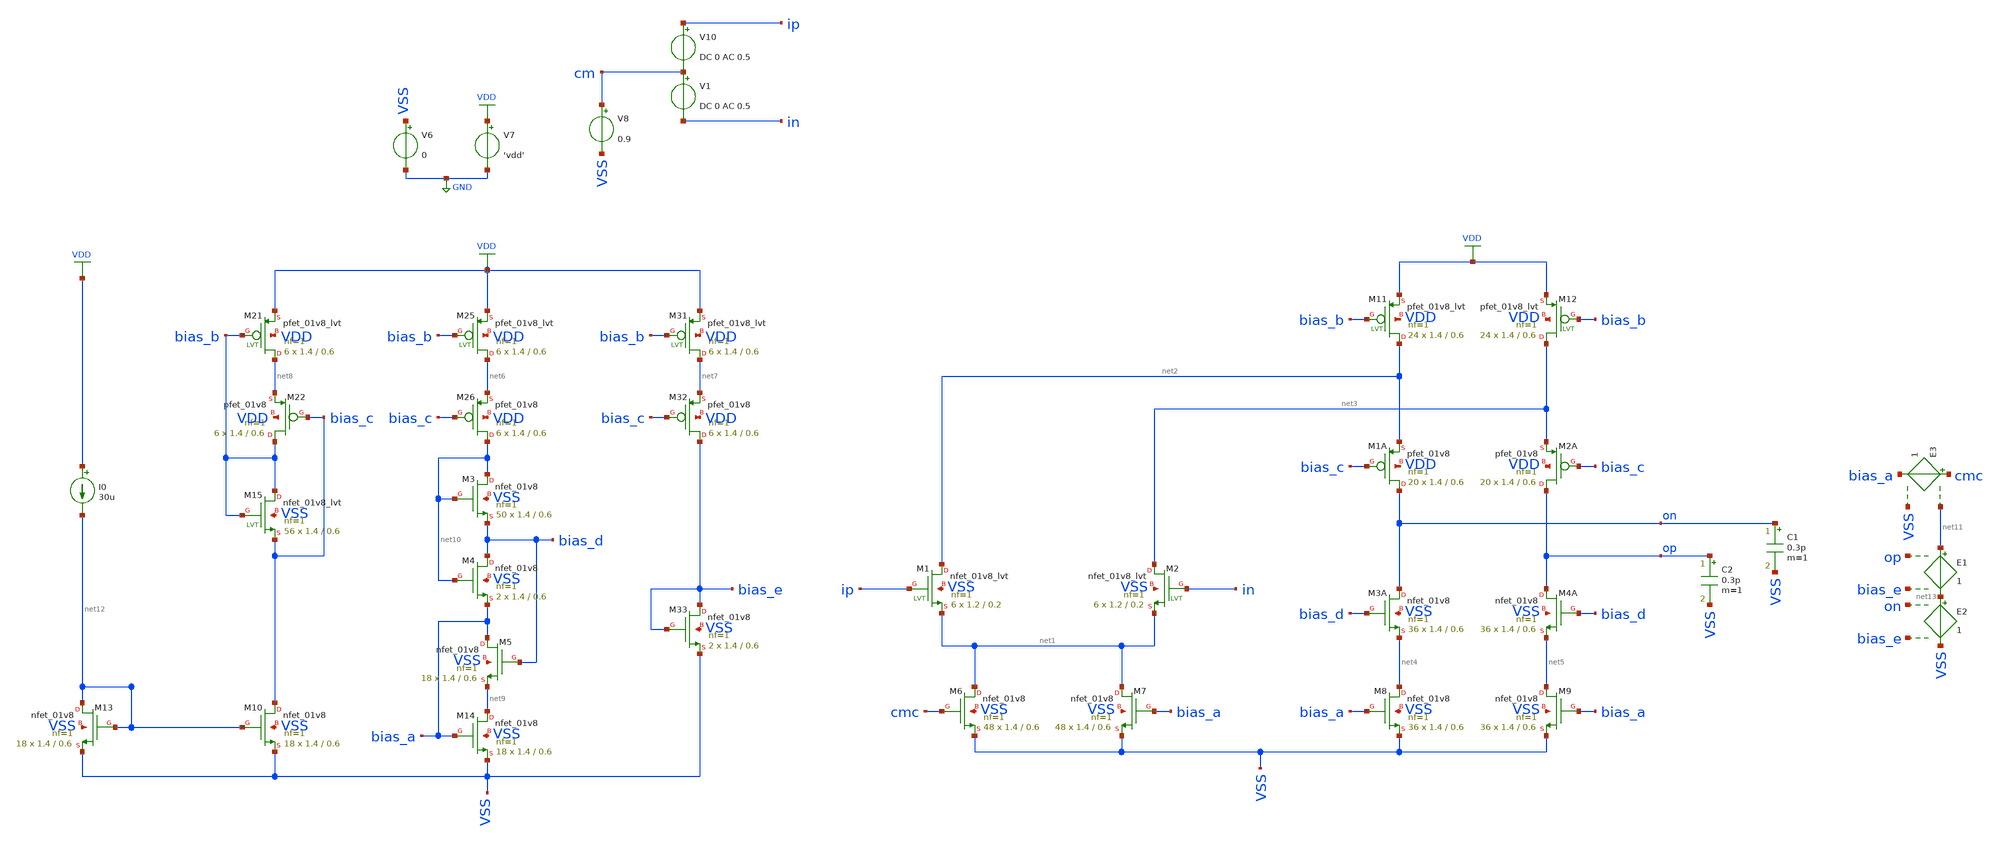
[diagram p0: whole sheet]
** sch_path: verification/schematic/folded_cascode_pvt_tb.sch
**.subckt folded_cascode_pvt_tb
XM1 net2 ip net1 VSS sky130_fd_pr__nfet_01v8_lvt L=0.2 W=1.2 nf=1 ad='int((nf+1)/2) * W/nf * 0.29' as='int((nf+2)/2) * W/nf * 0.29'
+ pd='2*int((nf+1)/2) * (W/nf + 0.29)' ps='2*int((nf+2)/2) * (W/nf + 0.29)' nrd='0.29 / W' nrs='0.29 / W'
+ sa=0 sb=0 sd=0 mult=6 m=6
XM2 net3 in net1 VSS sky130_fd_pr__nfet_01v8_lvt L=0.2 W=1.2 nf=1 ad='int((nf+1)/2) * W/nf * 0.29' as='int((nf+2)/2) * W/nf * 0.29'
+ pd='2*int((nf+1)/2) * (W/nf + 0.29)' ps='2*int((nf+2)/2) * (W/nf + 0.29)' nrd='0.29 / W' nrs='0.29 / W'
+ sa=0 sb=0 sd=0 mult=6 m=6
XM6 net1 cmc VSS VSS sky130_fd_pr__nfet_01v8 L=0.6 W=1.4 nf=1 ad='int((nf+1)/2) * W/nf * 0.29' as='int((nf+2)/2) * W/nf * 0.29'
+ pd='2*int((nf+1)/2) * (W/nf + 0.29)' ps='2*int((nf+2)/2) * (W/nf + 0.29)' nrd='0.29 / W' nrs='0.29 / W'
+ sa=0 sb=0 sd=0 mult=48 m=48
XM7 net1 bias_a VSS VSS sky130_fd_pr__nfet_01v8 L=0.6 W=1.4 nf=1 ad='int((nf+1)/2) * W/nf * 0.29' as='int((nf+2)/2) * W/nf * 0.29'
+ pd='2*int((nf+1)/2) * (W/nf + 0.29)' ps='2*int((nf+2)/2) * (W/nf + 0.29)' nrd='0.29 / W' nrs='0.29 / W'
+ sa=0 sb=0 sd=0 mult=48 m=48
XM11 net2 bias_b VDD VDD sky130_fd_pr__pfet_01v8_lvt L=0.6 W=1.4 nf=1 ad='int((nf+1)/2) * W/nf * 0.29'
+ as='int((nf+2)/2) * W/nf * 0.29' pd='2*int((nf+1)/2) * (W/nf + 0.29)' ps='2*int((nf+2)/2) * (W/nf + 0.29)'
+ nrd='0.29 / W' nrs='0.29 / W' sa=0 sb=0 sd=0 mult=24 m=24
XM12 net3 bias_b VDD VDD sky130_fd_pr__pfet_01v8_lvt L=0.6 W=1.4 nf=1 ad='int((nf+1)/2) * W/nf * 0.29'
+ as='int((nf+2)/2) * W/nf * 0.29' pd='2*int((nf+1)/2) * (W/nf + 0.29)' ps='2*int((nf+2)/2) * (W/nf + 0.29)'
+ nrd='0.29 / W' nrs='0.29 / W' sa=0 sb=0 sd=0 mult=24 m=24
XM1A on bias_c net2 VDD sky130_fd_pr__pfet_01v8 L=0.6 W=1.4 nf=1 ad='int((nf+1)/2) * W/nf * 0.29' as='int((nf+2)/2) * W/nf * 0.29'
+ pd='2*int((nf+1)/2) * (W/nf + 0.29)' ps='2*int((nf+2)/2) * (W/nf + 0.29)' nrd='0.29 / W' nrs='0.29 / W'
+ sa=0 sb=0 sd=0 mult=20 m=20
XM2A op bias_c net3 VDD sky130_fd_pr__pfet_01v8 L=0.6 W=1.4 nf=1 ad='int((nf+1)/2) * W/nf * 0.29' as='int((nf+2)/2) * W/nf * 0.29'
+ pd='2*int((nf+1)/2) * (W/nf + 0.29)' ps='2*int((nf+2)/2) * (W/nf + 0.29)' nrd='0.29 / W' nrs='0.29 / W'
+ sa=0 sb=0 sd=0 mult=20 m=20
XM3A on bias_d net4 VSS sky130_fd_pr__nfet_01v8 L=0.6 W=1.4 nf=1 ad='int((nf+1)/2) * W/nf * 0.29' as='int((nf+2)/2) * W/nf * 0.29'
+ pd='2*int((nf+1)/2) * (W/nf + 0.29)' ps='2*int((nf+2)/2) * (W/nf + 0.29)' nrd='0.29 / W' nrs='0.29 / W'
+ sa=0 sb=0 sd=0 mult=36 m=36
XM4A op bias_d net5 VSS sky130_fd_pr__nfet_01v8 L=0.6 W=1.4 nf=1 ad='int((nf+1)/2) * W/nf * 0.29' as='int((nf+2)/2) * W/nf * 0.29'
+ pd='2*int((nf+1)/2) * (W/nf + 0.29)' ps='2*int((nf+2)/2) * (W/nf + 0.29)' nrd='0.29 / W' nrs='0.29 / W'
+ sa=0 sb=0 sd=0 mult=36 m=36
XM8 net4 bias_a VSS VSS sky130_fd_pr__nfet_01v8 L=0.6 W=1.4 nf=1 ad='int((nf+1)/2) * W/nf * 0.29' as='int((nf+2)/2) * W/nf * 0.29'
+ pd='2*int((nf+1)/2) * (W/nf + 0.29)' ps='2*int((nf+2)/2) * (W/nf + 0.29)' nrd='0.29 / W' nrs='0.29 / W'
+ sa=0 sb=0 sd=0 mult=36 m=36
XM9 net5 bias_a VSS VSS sky130_fd_pr__nfet_01v8 L=0.6 W=1.4 nf=1 ad='int((nf+1)/2) * W/nf * 0.29' as='int((nf+2)/2) * W/nf * 0.29'
+ pd='2*int((nf+1)/2) * (W/nf + 0.29)' ps='2*int((nf+2)/2) * (W/nf + 0.29)' nrd='0.29 / W' nrs='0.29 / W'
+ sa=0 sb=0 sd=0 mult=36 m=36
V6 VSS GND 0
V7 VDD GND 'vdd'
V8 cm VSS 0.9
V10 ip cm DC 0 AC 0.5
V1 cm in DC 0 AC 0.5
XM22 bias_b bias_c net8 VDD sky130_fd_pr__pfet_01v8 L=0.6 W=1.4 nf=1 ad='int((nf+1)/2) * W/nf * 0.29'
+ as='int((nf+2)/2) * W/nf * 0.29' pd='2*int((nf+1)/2) * (W/nf + 0.29)' ps='2*int((nf+2)/2) * (W/nf + 0.29)'
+ nrd='0.29 / W' nrs='0.29 / W' sa=0 sb=0 sd=0 mult=6 m=6
XM26 net10 bias_c net6 VDD sky130_fd_pr__pfet_01v8 L=0.6 W=1.4 nf=1 ad='int((nf+1)/2) * W/nf * 0.29'
+ as='int((nf+2)/2) * W/nf * 0.29' pd='2*int((nf+1)/2) * (W/nf + 0.29)' ps='2*int((nf+2)/2) * (W/nf + 0.29)'
+ nrd='0.29 / W' nrs='0.29 / W' sa=0 sb=0 sd=0 mult=6 m=6
XM32 bias_e bias_c net7 VDD sky130_fd_pr__pfet_01v8 L=0.6 W=1.4 nf=1 ad='int((nf+1)/2) * W/nf * 0.29'
+ as='int((nf+2)/2) * W/nf * 0.29' pd='2*int((nf+1)/2) * (W/nf + 0.29)' ps='2*int((nf+2)/2) * (W/nf + 0.29)'
+ nrd='0.29 / W' nrs='0.29 / W' sa=0 sb=0 sd=0 mult=6 m=6
XM33 bias_e bias_e VSS VSS sky130_fd_pr__nfet_01v8 L=0.6 W=1.4 nf=1 ad='int((nf+1)/2) * W/nf * 0.29'
+ as='int((nf+2)/2) * W/nf * 0.29' pd='2*int((nf+1)/2) * (W/nf + 0.29)' ps='2*int((nf+2)/2) * (W/nf + 0.29)'
+ nrd='0.29 / W' nrs='0.29 / W' sa=0 sb=0 sd=0 mult=2 m=2
XM21 net8 bias_b VDD VDD sky130_fd_pr__pfet_01v8_lvt L=0.6 W=1.4 nf=1 ad='int((nf+1)/2) * W/nf * 0.29'
+ as='int((nf+2)/2) * W/nf * 0.29' pd='2*int((nf+1)/2) * (W/nf + 0.29)' ps='2*int((nf+2)/2) * (W/nf + 0.29)'
+ nrd='0.29 / W' nrs='0.29 / W' sa=0 sb=0 sd=0 mult=6 m=6
XM25 net6 bias_b VDD VDD sky130_fd_pr__pfet_01v8_lvt L=0.6 W=1.4 nf=1 ad='int((nf+1)/2) * W/nf * 0.29'
+ as='int((nf+2)/2) * W/nf * 0.29' pd='2*int((nf+1)/2) * (W/nf + 0.29)' ps='2*int((nf+2)/2) * (W/nf + 0.29)'
+ nrd='0.29 / W' nrs='0.29 / W' sa=0 sb=0 sd=0 mult=6 m=6
XM31 net7 bias_b VDD VDD sky130_fd_pr__pfet_01v8_lvt L=0.6 W=1.4 nf=1 ad='int((nf+1)/2) * W/nf * 0.29'
+ as='int((nf+2)/2) * W/nf * 0.29' pd='2*int((nf+1)/2) * (W/nf + 0.29)' ps='2*int((nf+2)/2) * (W/nf + 0.29)'
+ nrd='0.29 / W' nrs='0.29 / W' sa=0 sb=0 sd=0 mult=6 m=6
XM3 net10 net10 bias_d VSS sky130_fd_pr__nfet_01v8 L=0.6 W=1.4 nf=1 ad='int((nf+1)/2) * W/nf * 0.29'
+ as='int((nf+2)/2) * W/nf * 0.29' pd='2*int((nf+1)/2) * (W/nf + 0.29)' ps='2*int((nf+2)/2) * (W/nf + 0.29)'
+ nrd='0.29 / W' nrs='0.29 / W' sa=0 sb=0 sd=0 mult=50 m=50
XM4 bias_d net10 bias_a VSS sky130_fd_pr__nfet_01v8 L=0.6 W=1.4 nf=1 ad='int((nf+1)/2) * W/nf * 0.29'
+ as='int((nf+2)/2) * W/nf * 0.29' pd='2*int((nf+1)/2) * (W/nf + 0.29)' ps='2*int((nf+2)/2) * (W/nf + 0.29)'
+ nrd='0.29 / W' nrs='0.29 / W' sa=0 sb=0 sd=0 mult=2 m=2
XM5 bias_a bias_d net9 VSS sky130_fd_pr__nfet_01v8 L=0.6 W=1.4 nf=1 ad='int((nf+1)/2) * W/nf * 0.29'
+ as='int((nf+2)/2) * W/nf * 0.29' pd='2*int((nf+1)/2) * (W/nf + 0.29)' ps='2*int((nf+2)/2) * (W/nf + 0.29)'
+ nrd='0.29 / W' nrs='0.29 / W' sa=0 sb=0 sd=0 mult=18 m=18
XM14 net9 bias_a VSS VSS sky130_fd_pr__nfet_01v8 L=0.6 W=1.4 nf=1 ad='int((nf+1)/2) * W/nf * 0.29' as='int((nf+2)/2) * W/nf * 0.29'
+ pd='2*int((nf+1)/2) * (W/nf + 0.29)' ps='2*int((nf+2)/2) * (W/nf + 0.29)' nrd='0.29 / W' nrs='0.29 / W'
+ sa=0 sb=0 sd=0 mult=18 m=18
XM15 bias_b bias_b bias_c VSS sky130_fd_pr__nfet_01v8_lvt L=0.6 W=1.4 nf=1 ad='int((nf+1)/2) * W/nf * 0.29'
+ as='int((nf+2)/2) * W/nf * 0.29' pd='2*int((nf+1)/2) * (W/nf + 0.29)' ps='2*int((nf+2)/2) * (W/nf + 0.29)'
+ nrd='0.29 / W' nrs='0.29 / W' sa=0 sb=0 sd=0 mult=56 m=56
E1 net11 net13 op bias_e 1
E2 net13 VSS on bias_e 1
E3 cmc bias_a net11 VSS 1
C1 on VSS 0.3p m=1
C2 op VSS 0.3p m=1
XM10 bias_c net12 VSS VSS sky130_fd_pr__nfet_01v8 L=0.6 W=1.4 nf=1 ad='int((nf+1)/2) * W/nf * 0.29' as='int((nf+2)/2) * W/nf * 0.29'
+ pd='2*int((nf+1)/2) * (W/nf + 0.29)' ps='2*int((nf+2)/2) * (W/nf + 0.29)' nrd='0.29 / W' nrs='0.29 / W'
+ sa=0 sb=0 sd=0 mult=18 m=18
XM13 net12 net12 VSS VSS sky130_fd_pr__nfet_01v8 L=0.6 W=1.4 nf=1 ad='int((nf+1)/2) * W/nf * 0.29' as='int((nf+2)/2) * W/nf * 0.29'
+ pd='2*int((nf+1)/2) * (W/nf + 0.29)' ps='2*int((nf+2)/2) * (W/nf + 0.29)' nrd='0.29 / W' nrs='0.29 / W'
+ sa=0 sb=0 sd=0 mult=18 m=18
I0 VDD net12 30u
**** begin user architecture code

** opencircuitdesign pdks install
* Process Variation Test
.lib /farmshare/home/classes/ee/372/PDKs/open_pdks_1.0.310/sky130/sky130A/libs.tech/ngspice/sky130.lib.spice tt
*.lib /farmshare/home/classes/ee/372/PDKs/open_pdks_1.0.310/sky130/sky130A/libs.tech/ngspice/sky130.lib.spice ss
*.lib /farmshare/home/classes/ee/372/PDKs/open_pdks_1.0.310/sky130/sky130A/libs.tech/ngspice/sky130.lib.spice ff




.param vdd=1.8

.save all

* Process Variation test
* change the tt, ss, ff model in the TT_models
*.control
*    ac dec 20 1 1e10
*    let phase=180/PI*vp(op,on)
*    let gain_db = vdb(op,on)
*    meas ac dc_gain find gain_db at=20
*    meas ac unity_gain_frequency when gain_db=0
*    let gain_3db = dc_gain - 3
*    meas ac frequency_3db when gain_db=gain_3db
*    meas ac phase_at_0db find phase when gain_db=0
*    plot vdb(op,on)
*    plot 180/PI*vp(op,on)
*.endc

* Voltage test
*.ac dec 20 1 1e10
*.control
*    let supply = 1.62
*    while supply < 2
*        alterparam vdd = {$&supply}
*        reset
*        run
*        echo voltage_at_{$&supply}_V
*        let phase=180/PI*vp(op,on)
*        let gain_db = vdb(op,on)
*        meas ac dc_gain find gain_db at=20
*        meas ac unity_gain_frequency when gain_db=0
*        let gain_3db = dc_gain - 3
*        meas ac frequency_3db when gain_db=gain_3db
*        meas ac phase_at_0db find phase when gain_db=0
*        plot vdb(op,on) phase title voltage_at_{$&supply}_V
*        let supply = supply + 0.06
*    end
*.endc


* Temperature test
.ac dec 20 1 1e10
.control
    let temperature = -25
    while temperature < 100
        set temp = $&temperature
        run
        let phase=180/PI*vp(op,on)
        let gain_db = vdb(op,on)
        meas ac dc_gain find gain_db at=20
        meas ac unity_gain_frequency when gain_db=0
        let gain_3db = dc_gain - 3
        meas ac frequency_3db when gain_db=gain_3db
        meas ac phase_at_0db find phase when gain_db=0
        plot vdb(op,on) phase title temperature_at_{$&temperature}_degree
        let temperature = temperature + 10
    end
.endc


**** end user architecture code
**.ends
.GLOBAL VDD
.GLOBAL GND
.end
